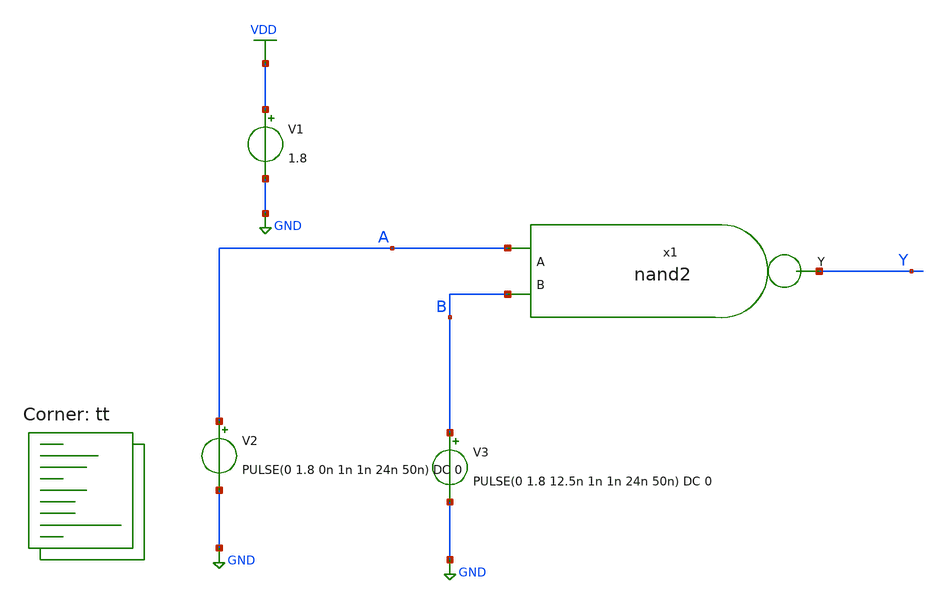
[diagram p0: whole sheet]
** sch_path: eng331lab_final/eng331lab_xschem/tb_nand2.sch
**.subckt tb_nand2
x1 A Y B nand2
V1 VDD GND 1.8
V2 A GND PULSE(0 1.8 0n 1n 1n 24n 50n) DC 0
V3 B GND PULSE(0 1.8 12.5n 1n 1n 24n 50n) DC 0
**** begin user architecture code

.control
  save all
  tran 10n 400n
  write tb_nand2.raw
  set appendwrite
.endc


.lib $::SKYWATER_MODELS/sky130.lib.spice tt
**** end user architecture code
**.ends

* expanding   symbol:  eng331lab_xschem/nand2.sym # of pins=3
** sym_path: eng331lab_final/eng331lab_xschem/nand2.sym
** sch_path: eng331lab_final/eng331lab_xschem/nand2.sch
.subckt nand2 A Y B
*.ipin A
*.ipin B
*.opin Y
XM1 Y A VDD VDD sky130_fd_pr__pfet_01v8 L=0.15 W=0.8 nf=1 ad='int((1 + 1)/2) * 0.8 / 1 * 0.29' as='int((1 + 2)/2) * 0.8 / 1 * 0.29'
+ pd='2*int((1 + 1)/2) * (0.8 / 1 + 0.29)' ps='2*int((1 + 2)/2) * (0.8 / 1 + 0.29)' nrd='0.29 / 0.8 ' nrs='0.29 / 0.8 '
+ sa=0 sb=0 sd=0 mult=1 m=1
XM2 Y B VDD VDD sky130_fd_pr__pfet_01v8 L=0.15 W=0.8 nf=1 ad='int((1 + 1)/2) * 0.8 / 1 * 0.29' as='int((1 + 2)/2) * 0.8 / 1 * 0.29'
+ pd='2*int((1 + 1)/2) * (0.8 / 1 + 0.29)' ps='2*int((1 + 2)/2) * (0.8 / 1 + 0.29)' nrd='0.29 / 0.8 ' nrs='0.29 / 0.8 '
+ sa=0 sb=0 sd=0 mult=1 m=1
XM3 Y A net1 GND sky130_fd_pr__nfet_01v8 L=0.15 W=1 nf=1 ad='int((1 + 1)/2) * 1 / 1 * 0.29' as='int((1 + 2)/2) * 1 / 1 * 0.29'
+ pd='2*int((1 + 1)/2) * (1 / 1 + 0.29)' ps='2*int((1 + 2)/2) * (1 / 1 + 0.29)' nrd='0.29 / 1 ' nrs='0.29 / 1 '
+ sa=0 sb=0 sd=0 mult=1 m=1
XM4 net1 B GND GND sky130_fd_pr__nfet_01v8 L=0.15 W=1 nf=1 ad='int((1 + 1)/2) * 1 / 1 * 0.29' as='int((1 + 2)/2) * 1 / 1 * 0.29'
+ pd='2*int((1 + 1)/2) * (1 / 1 + 0.29)' ps='2*int((1 + 2)/2) * (1 / 1 + 0.29)' nrd='0.29 / 1 ' nrs='0.29 / 1 '
+ sa=0 sb=0 sd=0 mult=1 m=1
.ends

.GLOBAL VDD
.GLOBAL GND
.end
